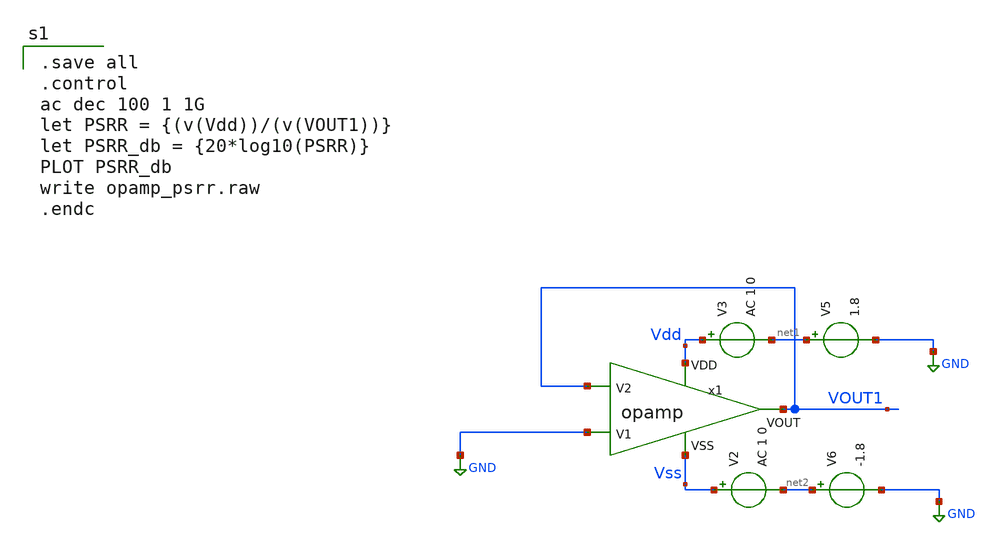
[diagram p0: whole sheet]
** sch_path: opamp_psrr.sch
**.subckt opamp_psrr
V2 Vss net2 AC 1 0
V3 Vdd net1 AC 1 0
x1 Vdd VOUT1 GND VOUT1 Vss opamp
V5 net1 GND 1.8
V6 net2 GND -1.8
**** begin user architecture code

.save all
.control
ac dec 100 1 1G
let PSRR = {(v(Vdd))/(v(VOUT1))}
let PSRR_db = {20*log10(PSRR)}
PLOT PSRR_db
write opamp_psrr.raw
.endc


** opencircuitdesign pdks install
.lib $::SKYWATER_MODELS/sky130.lib.spice tt


**** end user architecture code
**.ends

* expanding   symbol:  /foss/designs/FINAL_PROJECT_KTMDT/opamp.sym # of pins=5
** sym_path: /foss/designs/FINAL_PROJECT_KTMDT/opamp.sym
** sch_path: /foss/designs/FINAL_PROJECT_KTMDT/opamp.sch
.subckt opamp VDD V2 V1 VOUT VSS
*.ipin VSS
*.ipin VDD
*.ipin V2
*.ipin V1
*.opin VOUT
XM3 net4 V2 net1 VSS sky130_fd_pr__nfet_g5v0d10v5 L=1 W=17.45 nf=1 ad='int((nf+1)/2) * W/nf * 0.29' as='int((nf+2)/2) * W/nf * 0.29'
+ pd='2*int((nf+1)/2) * (W/nf + 0.29)' ps='2*int((nf+2)/2) * (W/nf + 0.29)' nrd='0.29 / W' nrs='0.29 / W'
+ sa=0 sb=0 sd=0 mult=1 m=1
XM1 net5 net4 VDD VDD sky130_fd_pr__pfet_g5v0d10v5 L=1 W=30 nf=1 ad='int((nf+1)/2) * W/nf * 0.29' as='int((nf+2)/2) * W/nf * 0.29'
+ pd='2*int((nf+1)/2) * (W/nf + 0.29)' ps='2*int((nf+2)/2) * (W/nf + 0.29)' nrd='0.29 / W' nrs='0.29 / W'
+ sa=0 sb=0 sd=0 mult=1 m=1
XM4 net5 V1 net1 VSS sky130_fd_pr__nfet_g5v0d10v5 L=1 W=17.45 nf=1 ad='int((nf+1)/2) * W/nf * 0.29' as='int((nf+2)/2) * W/nf * 0.29'
+ pd='2*int((nf+1)/2) * (W/nf + 0.29)' ps='2*int((nf+2)/2) * (W/nf + 0.29)' nrd='0.29 / W' nrs='0.29 / W'
+ sa=0 sb=0 sd=0 mult=1 m=1
XM6 net1 net6 VSS VSS sky130_fd_pr__nfet_g5v0d10v5 L=1 W=15.17 nf=1 ad='int((nf+1)/2) * W/nf * 0.29'
+ as='int((nf+2)/2) * W/nf * 0.29' pd='2*int((nf+1)/2) * (W/nf + 0.29)' ps='2*int((nf+2)/2) * (W/nf + 0.29)'
+ nrd='0.29 / W' nrs='0.29 / W' sa=0 sb=0 sd=0 mult=1 m=1
XM7 VOUT net6 VSS VSS sky130_fd_pr__nfet_g5v0d10v5 L=1 W=19 nf=1 ad='int((nf+1)/2) * W/nf * 0.29' as='int((nf+2)/2) * W/nf * 0.29'
+ pd='2*int((nf+1)/2) * (W/nf + 0.29)' ps='2*int((nf+2)/2) * (W/nf + 0.29)' nrd='0.29 / W' nrs='0.29 / W'
+ sa=0 sb=0 sd=0 mult=1 m=1
XM5 net6 net6 VSS VSS sky130_fd_pr__nfet_g5v0d10v5 L=1 W=15.17 nf=1 ad='int((nf+1)/2) * W/nf * 0.29'
+ as='int((nf+2)/2) * W/nf * 0.29' pd='2*int((nf+1)/2) * (W/nf + 0.29)' ps='2*int((nf+2)/2) * (W/nf + 0.29)'
+ nrd='0.29 / W' nrs='0.29 / W' sa=0 sb=0 sd=0 mult=1 m=1
XM2 net4 net4 VDD VDD sky130_fd_pr__pfet_g5v0d10v5 L=1 W=30 nf=1 ad='int((nf+1)/2) * W/nf * 0.29' as='int((nf+2)/2) * W/nf * 0.29'
+ pd='2*int((nf+1)/2) * (W/nf + 0.29)' ps='2*int((nf+2)/2) * (W/nf + 0.29)' nrd='0.29 / W' nrs='0.29 / W'
+ sa=0 sb=0 sd=0 mult=1 m=1
XM8 VOUT net5 VDD VDD sky130_fd_pr__pfet_g5v0d10v5 L=1 W=38 nf=1 ad='int((nf+1)/2) * W/nf * 0.29' as='int((nf+2)/2) * W/nf * 0.29'
+ pd='2*int((nf+1)/2) * (W/nf + 0.29)' ps='2*int((nf+2)/2) * (W/nf + 0.29)' nrd='0.29 / W' nrs='0.29 / W'
+ sa=0 sb=0 sd=0 mult=2 m=2
V_ibias net7 net6 0
.save i(v_ibias)
XR1 net2 VDD VSS sky130_fd_pr__res_high_po W=1 L=41.1 mult=1 m=1
XR2 net3 net2 VSS sky130_fd_pr__res_high_po W=1 L=41.1 mult=1 m=1
XR3 net7 net3 VSS sky130_fd_pr__res_high_po W=1 L=41.1 mult=1 m=1
XR4 net8 VOUT VSS sky130_fd_pr__res_high_po W=1 L=5 mult=1 m=1
XC1 net8 net5 sky130_fd_pr__cap_mim_m3_1 W=9 L=9 MF=2 m=2
.ends

.GLOBAL GND
.end
